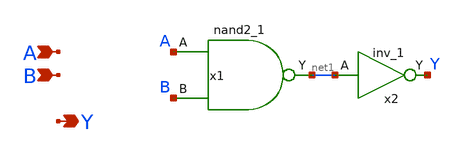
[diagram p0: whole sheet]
** sch_path: designs/libs/core_fpga/AND2_1/AND2_1.sch
**.subckt AND2_1 A B Y
*.ipin A
*.ipin B
*.opin Y
x1 A B VSSd VDDd VSSd VDDd net1 gf180mcu_fd_sc_mcu9t5v0__nand2_1
x2 net1 VSSd VDDd VSSd VDDd Y gf180mcu_fd_sc_mcu9t5v0__inv_1
**.ends
.end
